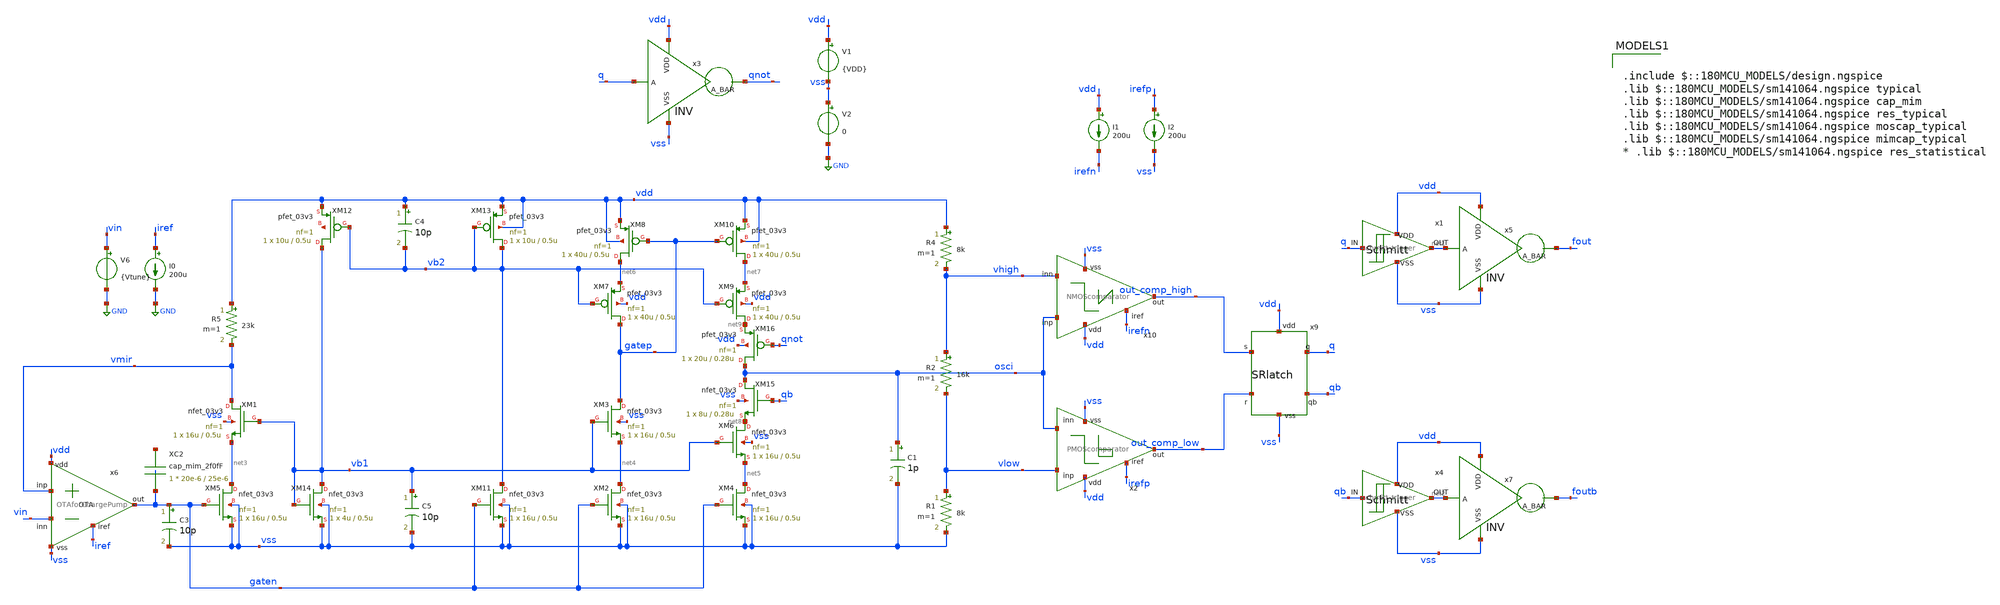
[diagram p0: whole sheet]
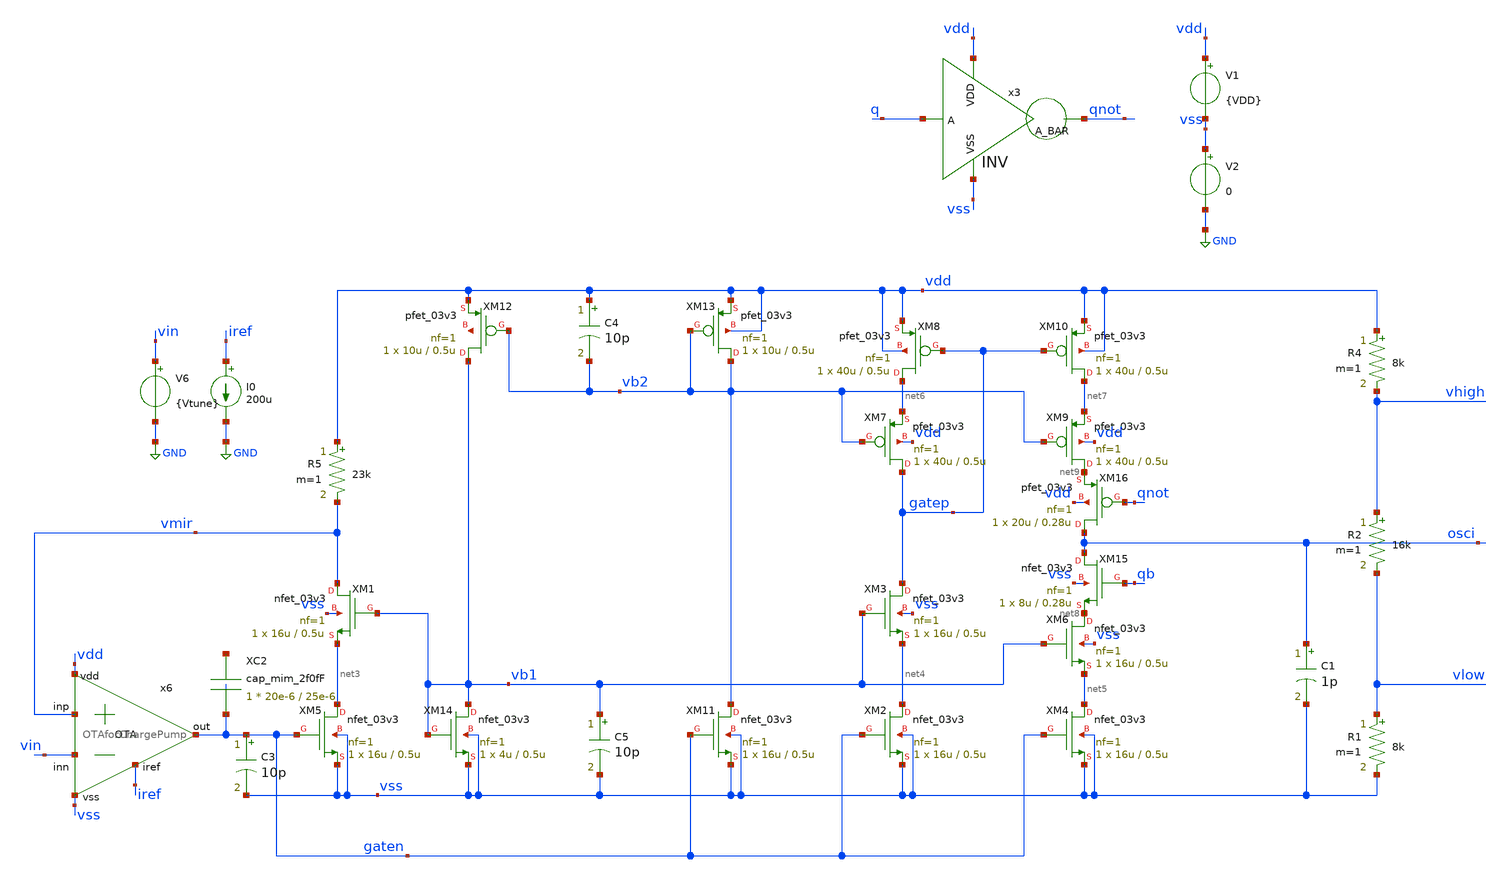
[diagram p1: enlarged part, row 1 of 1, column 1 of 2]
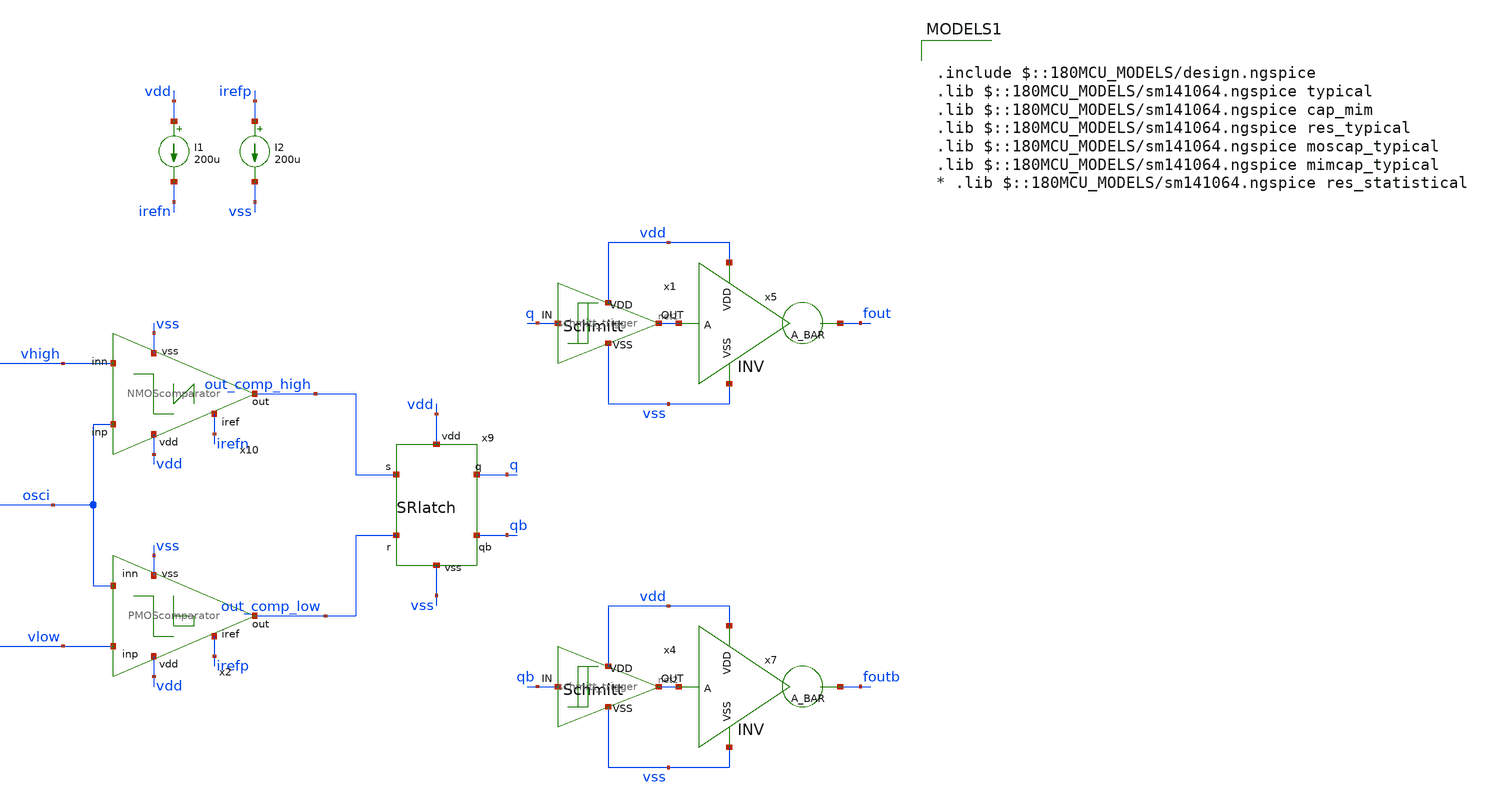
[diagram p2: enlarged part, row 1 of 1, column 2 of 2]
** sch_path: designs/libs/qw_core_analog_pkedit/RVCO_0812/RVCO_0812.sch
**.subckt RVCO_0812
V1 vdd vss {VDD}
V2 vss GND 0
C1 osci vss 1p m=1
I1 vdd irefn 200u
I2 irefp vss 200u
R1 vlow vss 8k m=1
R2 vhigh vlow 16k m=1
R4 vdd vhigh 8k m=1
x9 vdd out_comp_high q qb out_comp_low vss SRlatch
x2 vdd irefp vlow out_comp_low osci vss PMOScomparator
x10 vdd osci out_comp_high vhigh irefn vss NMOScomparator
x3 vdd q qnot vss INV
x1 q net1 vdd vss schmitt_trigger
x4 qb net2 vdd vss schmitt_trigger
x5 vdd net1 fout vss INV
x7 vdd net2 foutb vss INV
x6 vdd iref vmir vin gaten vss OTAforChargePump
XM5 net3 gaten vss vss nfet_03v3 L=0.5u W=16u nf=1 ad='int((nf+1)/2) * W/nf * 0.18u' as='int((nf+2)/2) * W/nf * 0.18u'
+ pd='2*int((nf+1)/2) * (W/nf + 0.18u)' ps='2*int((nf+2)/2) * (W/nf + 0.18u)' nrd='0.18u / W' nrs='0.18u / W'
+ sa=0 sb=0 sd=0 m=1
XM1 vmir vb1 net3 vss nfet_03v3 L=0.5u W=16u nf=1 ad='int((nf+1)/2) * W/nf * 0.18u' as='int((nf+2)/2) * W/nf * 0.18u'
+ pd='2*int((nf+1)/2) * (W/nf + 0.18u)' ps='2*int((nf+2)/2) * (W/nf + 0.18u)' nrd='0.18u / W' nrs='0.18u / W'
+ sa=0 sb=0 sd=0 m=1
XM2 net4 gaten vss vss nfet_03v3 L=0.5u W=16u nf=1 ad='int((nf+1)/2) * W/nf * 0.18u' as='int((nf+2)/2) * W/nf * 0.18u'
+ pd='2*int((nf+1)/2) * (W/nf + 0.18u)' ps='2*int((nf+2)/2) * (W/nf + 0.18u)' nrd='0.18u / W' nrs='0.18u / W'
+ sa=0 sb=0 sd=0 m=1
XM3 gatep vb1 net4 vss nfet_03v3 L=0.5u W=16u nf=1 ad='int((nf+1)/2) * W/nf * 0.18u' as='int((nf+2)/2) * W/nf * 0.18u'
+ pd='2*int((nf+1)/2) * (W/nf + 0.18u)' ps='2*int((nf+2)/2) * (W/nf + 0.18u)' nrd='0.18u / W' nrs='0.18u / W'
+ sa=0 sb=0 sd=0 m=1
XM4 net5 gaten vss vss nfet_03v3 L=0.5u W=16u nf=1 ad='int((nf+1)/2) * W/nf * 0.18u' as='int((nf+2)/2) * W/nf * 0.18u'
+ pd='2*int((nf+1)/2) * (W/nf + 0.18u)' ps='2*int((nf+2)/2) * (W/nf + 0.18u)' nrd='0.18u / W' nrs='0.18u / W'
+ sa=0 sb=0 sd=0 m=1
XM6 net8 vb1 net5 vss nfet_03v3 L=0.5u W=16u nf=1 ad='int((nf+1)/2) * W/nf * 0.18u' as='int((nf+2)/2) * W/nf * 0.18u'
+ pd='2*int((nf+1)/2) * (W/nf + 0.18u)' ps='2*int((nf+2)/2) * (W/nf + 0.18u)' nrd='0.18u / W' nrs='0.18u / W'
+ sa=0 sb=0 sd=0 m=1
XM7 gatep vb2 net6 vdd pfet_03v3 L=0.5u W=40u nf=1 ad='int((nf+1)/2) * W/nf * 0.18u' as='int((nf+2)/2) * W/nf * 0.18u'
+ pd='2*int((nf+1)/2) * (W/nf + 0.18u)' ps='2*int((nf+2)/2) * (W/nf + 0.18u)' nrd='0.18u / W' nrs='0.18u / W'
+ sa=0 sb=0 sd=0 m=1
XM8 net6 gatep vdd vdd pfet_03v3 L=0.5u W=40u nf=1 ad='int((nf+1)/2) * W/nf * 0.18u' as='int((nf+2)/2) * W/nf * 0.18u'
+ pd='2*int((nf+1)/2) * (W/nf + 0.18u)' ps='2*int((nf+2)/2) * (W/nf + 0.18u)' nrd='0.18u / W' nrs='0.18u / W'
+ sa=0 sb=0 sd=0 m=1
XM9 net9 vb2 net7 vdd pfet_03v3 L=0.5u W=40u nf=1 ad='int((nf+1)/2) * W/nf * 0.18u' as='int((nf+2)/2) * W/nf * 0.18u'
+ pd='2*int((nf+1)/2) * (W/nf + 0.18u)' ps='2*int((nf+2)/2) * (W/nf + 0.18u)' nrd='0.18u / W' nrs='0.18u / W'
+ sa=0 sb=0 sd=0 m=1
XM10 net7 gatep vdd vdd pfet_03v3 L=0.5u W=40u nf=1 ad='int((nf+1)/2) * W/nf * 0.18u' as='int((nf+2)/2) * W/nf * 0.18u'
+ pd='2*int((nf+1)/2) * (W/nf + 0.18u)' ps='2*int((nf+2)/2) * (W/nf + 0.18u)' nrd='0.18u / W' nrs='0.18u / W'
+ sa=0 sb=0 sd=0 m=1
R5 vdd vmir 23k m=1
XM11 vb2 gaten vss vss nfet_03v3 L=0.5u W=16u nf=1 ad='int((nf+1)/2) * W/nf * 0.18u' as='int((nf+2)/2) * W/nf * 0.18u'
+ pd='2*int((nf+1)/2) * (W/nf + 0.18u)' ps='2*int((nf+2)/2) * (W/nf + 0.18u)' nrd='0.18u / W' nrs='0.18u / W'
+ sa=0 sb=0 sd=0 m=1
XM12 vb1 vb2 vdd net10 pfet_03v3 L=0.5u W=10u nf=1 ad='int((nf+1)/2) * W/nf * 0.18u' as='int((nf+2)/2) * W/nf * 0.18u'
+ pd='2*int((nf+1)/2) * (W/nf + 0.18u)' ps='2*int((nf+2)/2) * (W/nf + 0.18u)' nrd='0.18u / W' nrs='0.18u / W'
+ sa=0 sb=0 sd=0 m=1
XM13 vb2 vb2 vdd vdd pfet_03v3 L=0.5u W=10u nf=1 ad='int((nf+1)/2) * W/nf * 0.18u' as='int((nf+2)/2) * W/nf * 0.18u'
+ pd='2*int((nf+1)/2) * (W/nf + 0.18u)' ps='2*int((nf+2)/2) * (W/nf + 0.18u)' nrd='0.18u / W' nrs='0.18u / W'
+ sa=0 sb=0 sd=0 m=1
XM14 vb1 vb1 vss vss nfet_03v3 L=0.5u W=4u nf=1 ad='int((nf+1)/2) * W/nf * 0.18u' as='int((nf+2)/2) * W/nf * 0.18u'
+ pd='2*int((nf+1)/2) * (W/nf + 0.18u)' ps='2*int((nf+2)/2) * (W/nf + 0.18u)' nrd='0.18u / W' nrs='0.18u / W'
+ sa=0 sb=0 sd=0 m=1
XM15 osci qb net8 vss nfet_03v3 L=0.28u W=8u nf=1 ad='int((nf+1)/2) * W/nf * 0.18u' as='int((nf+2)/2) * W/nf * 0.18u'
+ pd='2*int((nf+1)/2) * (W/nf + 0.18u)' ps='2*int((nf+2)/2) * (W/nf + 0.18u)' nrd='0.18u / W' nrs='0.18u / W'
+ sa=0 sb=0 sd=0 m=1
XM16 osci qnot net9 vdd pfet_03v3 L=0.28u W=20u nf=1 ad='int((nf+1)/2) * W/nf * 0.18u' as='int((nf+2)/2) * W/nf * 0.18u'
+ pd='2*int((nf+1)/2) * (W/nf + 0.18u)' ps='2*int((nf+2)/2) * (W/nf + 0.18u)' nrd='0.18u / W' nrs='0.18u / W'
+ sa=0 sb=0 sd=0 m=1
V6 vin GND {Vtune}
I0 iref GND 200u
XC2 net11 gaten cap_mim_2f0fF c_width=20e-6 c_length=25e-6 m=1
C3 gaten vss 10p m=1
C4 vdd vb2 10p m=1
C5 vb1 vss 10p m=1
**** begin user architecture code


* .param par_vth=0 par_k=0 par_l=0 par_w=0 par_leff=0 par_weff=0 p_sqrtarea=0 var_k=0 var_vth=0
.param VDD = 3.3 Vtune = {VDD/2}
.control
save all

**OP
**show all > op.log
**show all

** Source settings
**alter @V5[PULSE] = [ 1.64 1.66 20n 0.1n 0.1n 19.98n 40n 0 ]
**alter @V4[PULSE] = [ 1.66 1.64 20n 0.1n 0.1n 19.98n 40n 0 ]
**alter @V3[PULSE] = [ 0 3.3 10n 0.01n 0.01n 9.98n 20n 0 ]
**alter @V4[PULSE] = [ 0 3.3 50u 0.1u 0.1u 49.8u 100u 0 ]
alter @V1[PULSE] = [ 0 3.3 5n 1n 1n 49.998u 100u 0 ]

** Simulation settings

tran .1n 20u

write RVCO_0812.raw
.endc



.include $::180MCU_MODELS/design.ngspice
.lib $::180MCU_MODELS/sm141064.ngspice typical
.lib $::180MCU_MODELS/sm141064.ngspice cap_mim
.lib $::180MCU_MODELS/sm141064.ngspice res_typical
.lib $::180MCU_MODELS/sm141064.ngspice moscap_typical
.lib $::180MCU_MODELS/sm141064.ngspice mimcap_typical
* .lib $::180MCU_MODELS/sm141064.ngspice res_statistical

**** end user architecture code
**.ends
.GLOBAL GND
.end
